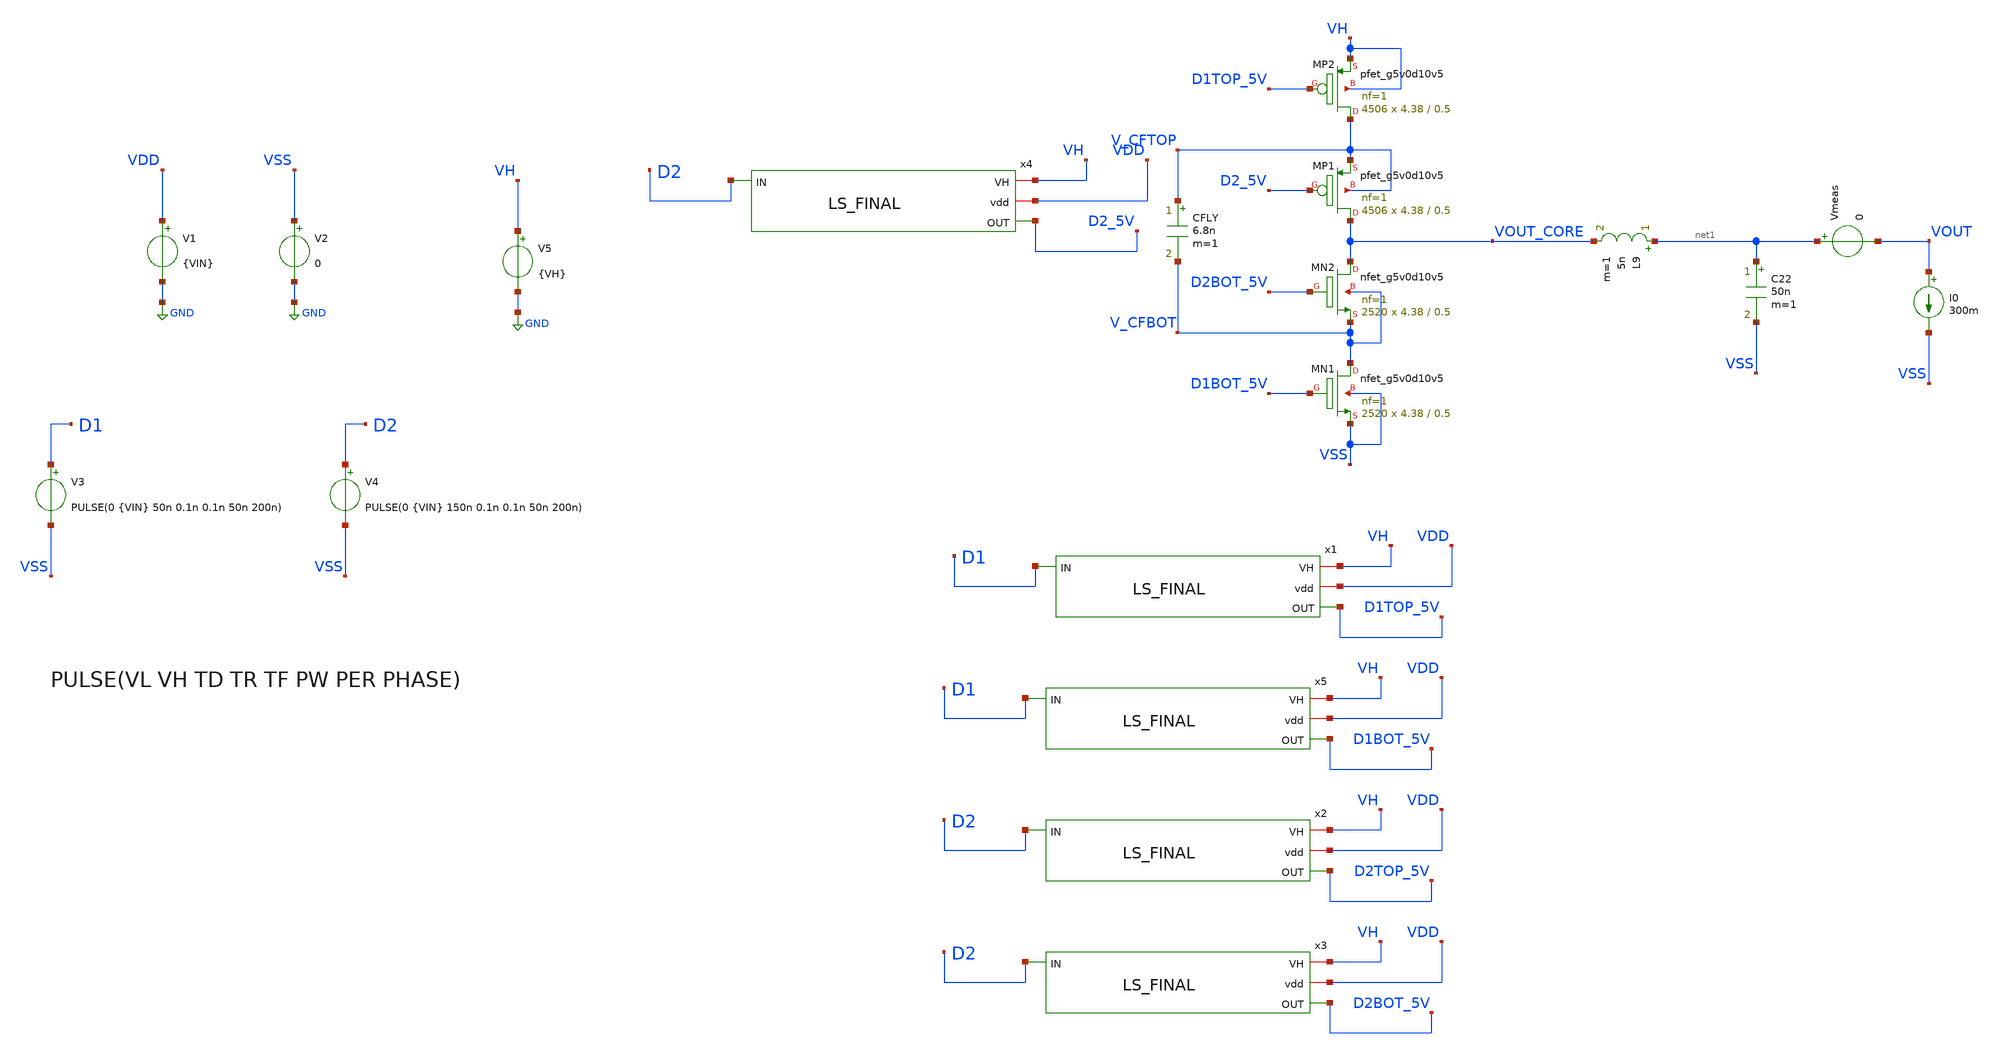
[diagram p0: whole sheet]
** sch_path: xschem/dev_switches/DCDC_5V_FINAL/DCDC_v1p4_5MHz_NMOS_PMOS_sng.sch
**.subckt DCDC_v1p4_5MHz_NMOS_PMOS_sng
XMN2 VOUT_CORE D2BOT_5V V_CFBOT V_CFBOT sky130_fd_pr__nfet_g5v0d10v5 L=0.5 W=4.38 nf=1 ad='int((nf+1)/2) * W/nf * 0.29'
+ as='int((nf+2)/2) * W/nf * 0.29' pd='2*int((nf+1)/2) * (W/nf + 0.29)' ps='2*int((nf+2)/2) * (W/nf + 0.29)'
+ nrd='0.29 / W' nrs='0.29 / W' sa=0 sb=0 sd=0 mult=2520 m=2520
XMN1 V_CFBOT D1BOT_5V VSS VSS sky130_fd_pr__nfet_g5v0d10v5 L=0.5 W=4.38 nf=1 ad='int((nf+1)/2) * W/nf * 0.29'
+ as='int((nf+2)/2) * W/nf * 0.29' pd='2*int((nf+1)/2) * (W/nf + 0.29)' ps='2*int((nf+2)/2) * (W/nf + 0.29)'
+ nrd='0.29 / W' nrs='0.29 / W' sa=0 sb=0 sd=0 mult=2520 m=2520
CFLY V_CFTOP V_CFBOT 6.8n m=1
V1 VDD GND {VIN}
V3 D1 VSS PULSE(0 {VIN} 50n 0.1n 0.1n 50n 200n)
V2 VSS GND 0
V4 D2 VSS PULSE(0 {VIN} 150n 0.1n 0.1n 50n 200n)
L9 net1 VOUT_CORE 5n m=1
C22 net1 VSS 50n m=1
V5 VH GND {VH}
XMP2 V_CFTOP D1TOP_5V VH VH sky130_fd_pr__pfet_g5v0d10v5 L=0.5 W=4.38 nf=1 ad='int((nf+1)/2) * W/nf * 0.29'
+ as='int((nf+2)/2) * W/nf * 0.29' pd='2*int((nf+1)/2) * (W/nf + 0.29)' ps='2*int((nf+2)/2) * (W/nf + 0.29)'
+ nrd='0.29 / W' nrs='0.29 / W' sa=0 sb=0 sd=0 mult=4506 m=4506
XMP1 VOUT_CORE D2_5V V_CFTOP V_CFTOP sky130_fd_pr__pfet_g5v0d10v5 L=0.5 W=4.38 nf=1 ad='int((nf+1)/2) * W/nf * 0.29'
+ as='int((nf+2)/2) * W/nf * 0.29' pd='2*int((nf+1)/2) * (W/nf + 0.29)' ps='2*int((nf+2)/2) * (W/nf + 0.29)'
+ nrd='0.29 / W' nrs='0.29 / W' sa=0 sb=0 sd=0 mult=4506 m=4506
x1 VH VDD D1TOP_5V D1 LS_FINAL
x2 VH VDD D2TOP_5V D2 LS_FINAL
x3 VH VDD D2BOT_5V D2 LS_FINAL
x4 VH VDD D2_5V D2 LS_FINAL
x5 VH VDD D1BOT_5V D1 LS_FINAL
I0 VOUT VSS 300m
Vmeas net1 VOUT 0
**** begin user architecture code


.param VIN = 1.8
.param VH = 5
.param RL = 50
.option scale=1e-6
*.option temp=70
.ic v(V_CFTOP) = VIN/2
.ic v(vout)=0
.ic v(V_CFBOT) = 0
*.probe vd(MP2:G:S)
*.save all
*.save v(d1) v(d2) v(d1top_5v) v(d2_5v) v(d2bot_5v) v(d1bot_5v) v(vout) v(vout_core) v(vdd) v(vh) i(v1) i(v5) i(vmeas) v(v_cftop,v_cfbot)
.save v(d1) v(d2) v(vout) v(vout_core) v(vdd) v(vh) i(v1) i(v5) i(vmeas) v(v_cftop,v_cfbot) v(d1top_5v,v_cftop) v(d2_5v,vout_core) v(d2bot_5v,v_cfbot) v(d1bot_5v,VSS)
.param mc_mm_switch=0
*.lib /home/jorge/Documents/Postdoc/share/pdk/sky130A/libs.tech/ngspice/sky130.lib.spice tt
*.lib /usr/share/pdk/sky130A/libs.tech/ngspice/sky130.lib.spice ss
.lib /foss/pdk/sky130A/libs.tech/ngspice/sky130.lib.spice TT
*.include /usr/share/pdk/sky130A/libs.ref/sky130_fd_sc_hvl/spice/sky130_fd_sc_hvl.spice
*.include /home/jorge/Documents/Postdoc/share/pdk/sky130A/libs.ref/sky130_fd_sc_hvl/spice/sky130_fd_sc_hvl.spice
.options savecurrents
.control
*save all
tran 100n 20u
write DCDC_v1p4_5MHz_NMOS_PMOS.raw
*wrdata
*+ ~/Documents/Postdoc/chipathon2022/3LFCC_AC3E/xschem/dev_switches/DCDC_5V_FINAL/3LFCC_v1p4.txt tran.v(vout) tran.i(vmeas) tran.v(vdd) tran.i(v1) tran.v(vh) tran.i(v5)
wrdata /foss/designs/personal/3LFCC_AC3E/xschem/dev_switches/DCDC_5V_FINAL/3LFCC_v1p4.txt
+ tran.v(vout) tran.i(v5) tran.i(v1)

*plot v(d1top_5v) v(d2_5v)
*plot v(d2bot_5v) v(d1bot_5v)
*plot v(v_cftop,v_cfbot) v(vout)
plot v(d1top_5v,v_cftop)
plot v(d2_5v,vout_core)
plot v(d2bot_5v,v_cfbot)
plot v(d1bot_5v,VSS)




*plot v(d1top_5v) v(d2_5v) v(d2bot_5v) v(d1bot_5v) v(v_cftop,v_cfbot) v(vout)
*plot v(v_cftop,v_cfbot) v(vout)
.endc


**** end user architecture code
**.ends

* expanding   symbol:  LS_FINAL.sym # of pins=4
** sym_path: xschem/dev_switches/DCDC_5V_FINAL/LS_FINAL.sym
** sch_path: xschem/dev_switches/DCDC_5V_FINAL/LS_FINAL.sch
.subckt LS_FINAL VH vdd OUT IN
*.ipin IN
*.iopin vdd
*.iopin VH
*.opin OUT
XM11 net1 IN vdd vdd sky130_fd_pr__pfet_01v8 L=0.15 W=5 nf=1 ad='int((nf+1)/2) * W/nf * 0.29' as='int((nf+2)/2) * W/nf * 0.29'
+ pd='2*int((nf+1)/2) * (W/nf + 0.29)' ps='2*int((nf+2)/2) * (W/nf + 0.29)' nrd='0.29 / W' nrs='0.29 / W'
+ sa=0 sb=0 sd=0 mult=1 m=1
XM12 net1 IN GND GND sky130_fd_pr__nfet_01v8 L=0.15 W=5 nf=1 ad='int((nf+1)/2) * W/nf * 0.29' as='int((nf+2)/2) * W/nf * 0.29'
+ pd='2*int((nf+1)/2) * (W/nf + 0.29)' ps='2*int((nf+2)/2) * (W/nf + 0.29)' nrd='0.29 / W' nrs='0.29 / W'
+ sa=0 sb=0 sd=0 mult=1 m=1
XM15 net2 net3 VH VH sky130_fd_pr__pfet_g5v0d10v5 L=0.5 W=2 nf=1 ad='int((nf+1)/2) * W/nf * 0.29' as='int((nf+2)/2) * W/nf * 0.29'
+ pd='2*int((nf+1)/2) * (W/nf + 0.29)' ps='2*int((nf+2)/2) * (W/nf + 0.29)' nrd='0.29 / W' nrs='0.29 / W'
+ sa=0 sb=0 sd=0 mult=1 m=1
XM14 net3 net2 VH VH sky130_fd_pr__pfet_g5v0d10v5 L=0.5 W=2 nf=1 ad='int((nf+1)/2) * W/nf * 0.29' as='int((nf+2)/2) * W/nf * 0.29'
+ pd='2*int((nf+1)/2) * (W/nf + 0.29)' ps='2*int((nf+2)/2) * (W/nf + 0.29)' nrd='0.29 / W' nrs='0.29 / W'
+ sa=0 sb=0 sd=0 mult=1 m=1
XM16 net4 net2 VH VH sky130_fd_pr__pfet_g5v0d10v5 L=0.5 W=10 nf=1 ad='int((nf+1)/2) * W/nf * 0.29' as='int((nf+2)/2) * W/nf * 0.29'
+ pd='2*int((nf+1)/2) * (W/nf + 0.29)' ps='2*int((nf+2)/2) * (W/nf + 0.29)' nrd='0.29 / W' nrs='0.29 / W'
+ sa=0 sb=0 sd=0 mult=10 m=10
XM18 net2 net1 GND GND sky130_fd_pr__nfet_g5v0d10v5 L=0.5 W=12 nf=1 ad='int((nf+1)/2) * W/nf * 0.29'
+ as='int((nf+2)/2) * W/nf * 0.29' pd='2*int((nf+1)/2) * (W/nf + 0.29)' ps='2*int((nf+2)/2) * (W/nf + 0.29)'
+ nrd='0.29 / W' nrs='0.29 / W' sa=0 sb=0 sd=0 mult=1 m=1
XM13 net3 IN GND GND sky130_fd_pr__nfet_g5v0d10v5 L=0.5 W=12 nf=1 ad='int((nf+1)/2) * W/nf * 0.29' as='int((nf+2)/2) * W/nf * 0.29'
+ pd='2*int((nf+1)/2) * (W/nf + 0.29)' ps='2*int((nf+2)/2) * (W/nf + 0.29)' nrd='0.29 / W' nrs='0.29 / W'
+ sa=0 sb=0 sd=0 mult=1 m=1
XM17 net4 IN GND GND sky130_fd_pr__nfet_g5v0d10v5 L=0.5 W=10 nf=1 ad='int((nf+1)/2) * W/nf * 0.29' as='int((nf+2)/2) * W/nf * 0.29'
+ pd='2*int((nf+1)/2) * (W/nf + 0.29)' ps='2*int((nf+2)/2) * (W/nf + 0.29)' nrd='0.29 / W' nrs='0.29 / W'
+ sa=0 sb=0 sd=0 mult=10 m=10
XM7 OUT net4 VH VH sky130_fd_pr__pfet_g5v0d10v5 L=0.5 W=10 nf=1 ad='int((nf+1)/2) * W/nf * 0.29' as='int((nf+2)/2) * W/nf * 0.29'
+ pd='2*int((nf+1)/2) * (W/nf + 0.29)' ps='2*int((nf+2)/2) * (W/nf + 0.29)' nrd='0.29 / W' nrs='0.29 / W'
+ sa=0 sb=0 sd=0 mult={multip} m={multip}
XM10 OUT net4 GND GND sky130_fd_pr__nfet_g5v0d10v5 L=0.5 W=10 nf=1 ad='int((nf+1)/2) * W/nf * 0.29' as='int((nf+2)/2) * W/nf * 0.29'
+ pd='2*int((nf+1)/2) * (W/nf + 0.29)' ps='2*int((nf+2)/2) * (W/nf + 0.29)' nrd='0.29 / W' nrs='0.29 / W'
+ sa=0 sb=0 sd=0 mult={multip} m={multip}
**** begin user architecture code

*
* Parameters

*.PARAM BAT=1.8
.PARAM W12=12 W45=2 LLS=0.5 multip=40
*.option scale=1e-6
*.options TEMP = 65.0

* Models
*.lib /foss/pdk/sky130A/libs.tech/ngspice/sky130.lib.spice TT

*Fuentes******
*VBAT VDD 0 DC BAT
*VHIGH VH 0 DC 5
*vin IN 0 dc 0 PULSE (0 BAT .1n .1n .1n 10n 20n)

*COUT OUT 0 20p


*.options savecurrents
*.save all
*+ @M.XM12.msky130_fd_pr_nfet_01v8[id]

*.control
*tran 0.1n 100n
*plot v(IN) v(LS1) v(OUT) v(net6) i(@M.XM12.msky130_fd_pr_nfet_01v8[id])
*write LS_FINAL.raw
*.endc
*.end
*

**** end user architecture code
.ends

.GLOBAL GND
.end
